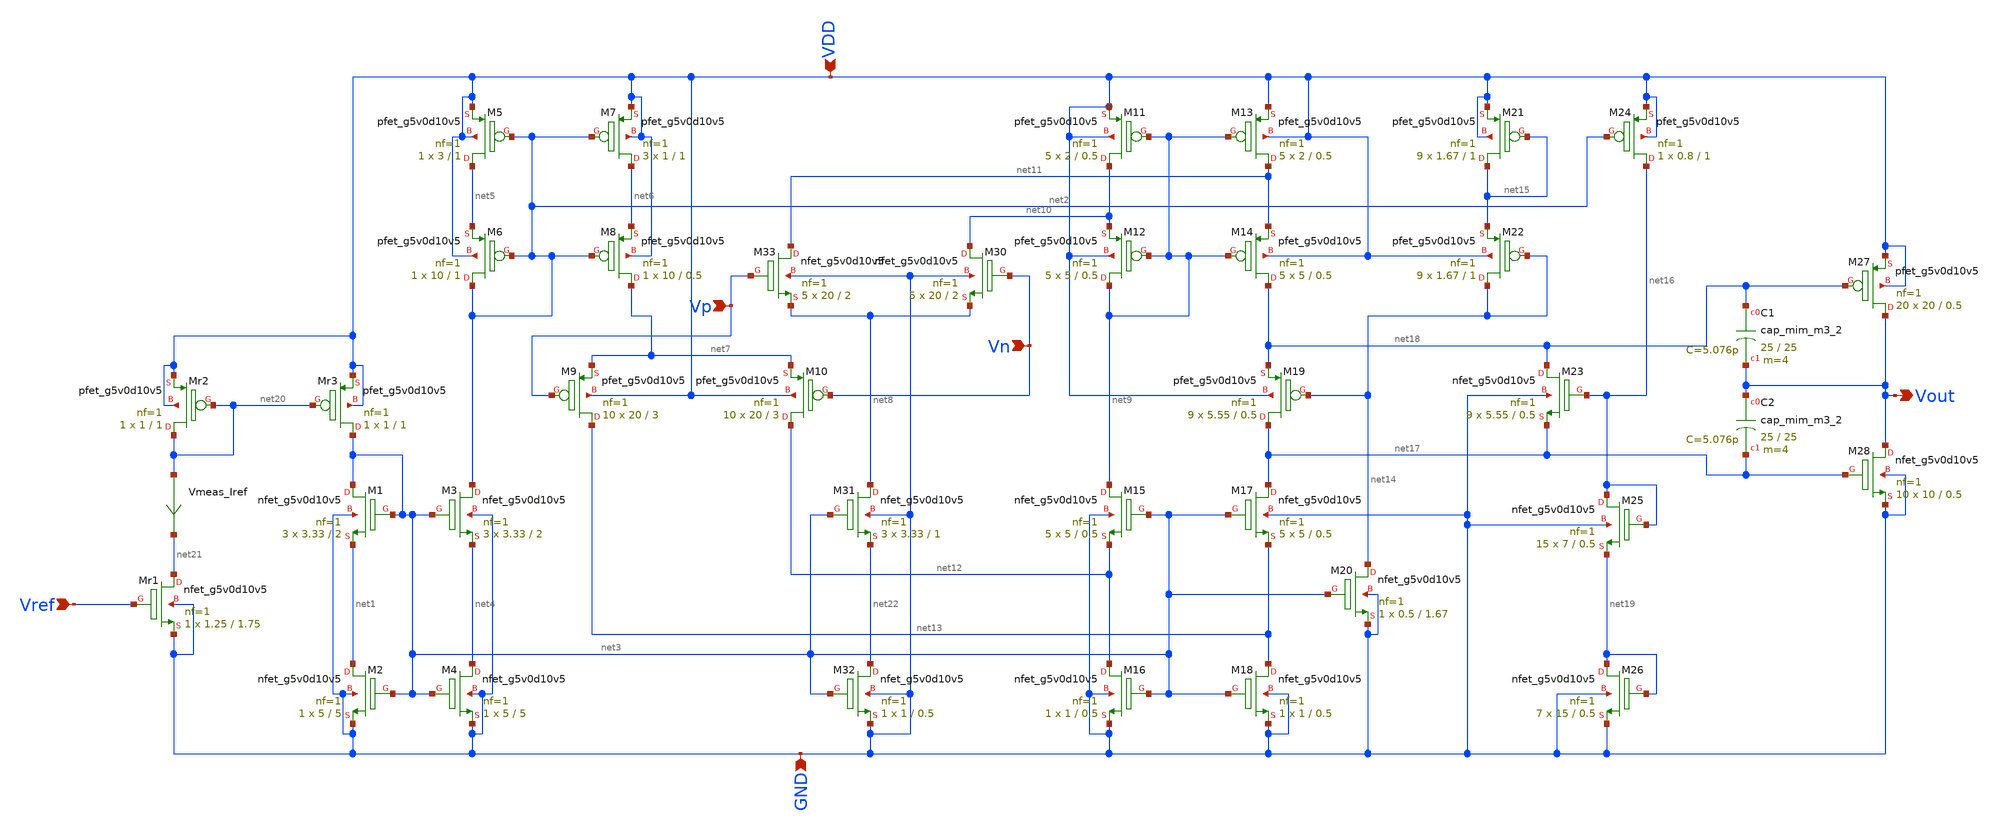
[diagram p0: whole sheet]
** sch_path: xschem/opamp_x.sch
**.subckt opamp_x Vref Vn Vp Vout VDD GND
*.ipin Vref
*.ipin Vn
*.ipin Vp
*.opin Vout
*.ipin VDD
*.ipin GND
XM1 net3 net3 net1 GND sky130_fd_pr__nfet_g5v0d10v5 L=2 W=3.33 nf=1 ad='int((1 + 1)/2) * 3.33 / 1 * 0.29'
+ as='int((1 + 2)/2) * 3.33 / 1 * 0.29' pd='2*int((1 + 1)/2) * (3.33 / 1 + 0.29)' ps='2*int((1 + 2)/2) * (3.33 / 1 + 0.29)'
+ nrd='0.29 / 3.33 ' nrs='0.29 / 3.33 ' sa=0 sb=0 sd=0 mult=3 m=3
XM2 net1 net3 GND GND sky130_fd_pr__nfet_g5v0d10v5 L=5 W=5 nf=1 ad='int((1 + 1)/2) * 5 / 1 * 0.29' as='int((1 + 2)/2) * 5 / 1 * 0.29'
+ pd='2*int((1 + 1)/2) * (5 / 1 + 0.29)' ps='2*int((1 + 2)/2) * (5 / 1 + 0.29)' nrd='0.29 / 5 ' nrs='0.29 / 5 '
+ sa=0 sb=0 sd=0 mult=1 m=1
XM3 net2 net3 net4 GND sky130_fd_pr__nfet_g5v0d10v5 L=2 W=3.33 nf=1 ad='int((1 + 1)/2) * 3.33 / 1 * 0.29'
+ as='int((1 + 2)/2) * 3.33 / 1 * 0.29' pd='2*int((1 + 1)/2) * (3.33 / 1 + 0.29)' ps='2*int((1 + 2)/2) * (3.33 / 1 + 0.29)'
+ nrd='0.29 / 3.33 ' nrs='0.29 / 3.33 ' sa=0 sb=0 sd=0 mult=3 m=3
XM4 net4 net3 GND GND sky130_fd_pr__nfet_g5v0d10v5 L=5 W=5 nf=1 ad='int((1 + 1)/2) * 5 / 1 * 0.29' as='int((1 + 2)/2) * 5 / 1 * 0.29'
+ pd='2*int((1 + 1)/2) * (5 / 1 + 0.29)' ps='2*int((1 + 2)/2) * (5 / 1 + 0.29)' nrd='0.29 / 5 ' nrs='0.29 / 5 '
+ sa=0 sb=0 sd=0 mult=1 m=1
XM5 net5 net2 VDD VDD sky130_fd_pr__pfet_g5v0d10v5 L=1 W=3 nf=1 ad='int((1 + 1)/2) * 3 / 1 * 0.29' as='int((1 + 2)/2) * 3 / 1 * 0.29'
+ pd='2*int((1 + 1)/2) * (3 / 1 + 0.29)' ps='2*int((1 + 2)/2) * (3 / 1 + 0.29)' nrd='0.29 / 3 ' nrs='0.29 / 3 '
+ sa=0 sb=0 sd=0 mult=1 m=1
XM6 net2 net2 net5 VDD sky130_fd_pr__pfet_g5v0d10v5 L=1 W=10 nf=1 ad='int((1 + 1)/2) * 10 / 1 * 0.29'
+ as='int((1 + 2)/2) * 10 / 1 * 0.29' pd='2*int((1 + 1)/2) * (10 / 1 + 0.29)' ps='2*int((1 + 2)/2) * (10 / 1 + 0.29)'
+ nrd='0.29 / 10 ' nrs='0.29 / 10 ' sa=0 sb=0 sd=0 mult=1 m=1
XM7 net6 net2 VDD VDD sky130_fd_pr__pfet_g5v0d10v5 L=1 W=1 nf=1 ad='int((1 + 1)/2) * 1 / 1 * 0.29' as='int((1 + 2)/2) * 1 / 1 * 0.29'
+ pd='2*int((1 + 1)/2) * (1 / 1 + 0.29)' ps='2*int((1 + 2)/2) * (1 / 1 + 0.29)' nrd='0.29 / 1 ' nrs='0.29 / 1 '
+ sa=0 sb=0 sd=0 mult=3 m=3
XM8 net7 net2 net6 VDD sky130_fd_pr__pfet_g5v0d10v5 L=0.5 W=10 nf=1 ad='int((1 + 1)/2) * 10 / 1 * 0.29'
+ as='int((1 + 2)/2) * 10 / 1 * 0.29' pd='2*int((1 + 1)/2) * (10 / 1 + 0.29)' ps='2*int((1 + 2)/2) * (10 / 1 + 0.29)'
+ nrd='0.29 / 10 ' nrs='0.29 / 10 ' sa=0 sb=0 sd=0 mult=1 m=1
XM9 net13 Vp net7 VDD sky130_fd_pr__pfet_g5v0d10v5 L=3 W=20 nf=1 ad='int((1 + 1)/2) * 20 / 1 * 0.29'
+ as='int((1 + 2)/2) * 20 / 1 * 0.29' pd='2*int((1 + 1)/2) * (20 / 1 + 0.29)' ps='2*int((1 + 2)/2) * (20 / 1 + 0.29)'
+ nrd='0.29 / 20 ' nrs='0.29 / 20 ' sa=0 sb=0 sd=0 mult=10 m=10
XM10 net12 Vn net7 VDD sky130_fd_pr__pfet_g5v0d10v5 L=3 W=20 nf=1 ad='int((1 + 1)/2) * 20 / 1 * 0.29'
+ as='int((1 + 2)/2) * 20 / 1 * 0.29' pd='2*int((1 + 1)/2) * (20 / 1 + 0.29)' ps='2*int((1 + 2)/2) * (20 / 1 + 0.29)'
+ nrd='0.29 / 20 ' nrs='0.29 / 20 ' sa=0 sb=0 sd=0 mult=10 m=10
XM11 net10 net9 VDD VDD sky130_fd_pr__pfet_g5v0d10v5 L=0.5 W=2 nf=1 ad='int((1 + 1)/2) * 2 / 1 * 0.29'
+ as='int((1 + 2)/2) * 2 / 1 * 0.29' pd='2*int((1 + 1)/2) * (2 / 1 + 0.29)' ps='2*int((1 + 2)/2) * (2 / 1 + 0.29)'
+ nrd='0.29 / 2 ' nrs='0.29 / 2 ' sa=0 sb=0 sd=0 mult=5 m=5
XM12 net9 net9 net10 VDD sky130_fd_pr__pfet_g5v0d10v5 L=0.5 W=5 nf=1 ad='int((1 + 1)/2) * 5 / 1 * 0.29'
+ as='int((1 + 2)/2) * 5 / 1 * 0.29' pd='2*int((1 + 1)/2) * (5 / 1 + 0.29)' ps='2*int((1 + 2)/2) * (5 / 1 + 0.29)'
+ nrd='0.29 / 5 ' nrs='0.29 / 5 ' sa=0 sb=0 sd=0 mult=5 m=5
XM13 net11 net9 VDD VDD sky130_fd_pr__pfet_g5v0d10v5 L=0.5 W=2 nf=1 ad='int((1 + 1)/2) * 2 / 1 * 0.29'
+ as='int((1 + 2)/2) * 2 / 1 * 0.29' pd='2*int((1 + 1)/2) * (2 / 1 + 0.29)' ps='2*int((1 + 2)/2) * (2 / 1 + 0.29)'
+ nrd='0.29 / 2 ' nrs='0.29 / 2 ' sa=0 sb=0 sd=0 mult=5 m=5
XM14 net18 net9 net11 VDD sky130_fd_pr__pfet_g5v0d10v5 L=0.5 W=5 nf=1 ad='int((1 + 1)/2) * 5 / 1 * 0.29'
+ as='int((1 + 2)/2) * 5 / 1 * 0.29' pd='2*int((1 + 1)/2) * (5 / 1 + 0.29)' ps='2*int((1 + 2)/2) * (5 / 1 + 0.29)'
+ nrd='0.29 / 5 ' nrs='0.29 / 5 ' sa=0 sb=0 sd=0 mult=5 m=5
XM15 net9 net3 net12 GND sky130_fd_pr__nfet_g5v0d10v5 L=0.5 W=5 nf=1 ad='int((1 + 1)/2) * 5 / 1 * 0.29'
+ as='int((1 + 2)/2) * 5 / 1 * 0.29' pd='2*int((1 + 1)/2) * (5 / 1 + 0.29)' ps='2*int((1 + 2)/2) * (5 / 1 + 0.29)'
+ nrd='0.29 / 5 ' nrs='0.29 / 5 ' sa=0 sb=0 sd=0 mult=5 m=5
XM16 net12 net3 GND GND sky130_fd_pr__nfet_g5v0d10v5 L=0.5 W=1 nf=1 ad='int((1 + 1)/2) * 1 / 1 * 0.29'
+ as='int((1 + 2)/2) * 1 / 1 * 0.29' pd='2*int((1 + 1)/2) * (1 / 1 + 0.29)' ps='2*int((1 + 2)/2) * (1 / 1 + 0.29)'
+ nrd='0.29 / 1 ' nrs='0.29 / 1 ' sa=0 sb=0 sd=0 mult=1 m=1
XM17 net17 net3 net13 GND sky130_fd_pr__nfet_g5v0d10v5 L=0.5 W=5 nf=1 ad='int((1 + 1)/2) * 5 / 1 * 0.29'
+ as='int((1 + 2)/2) * 5 / 1 * 0.29' pd='2*int((1 + 1)/2) * (5 / 1 + 0.29)' ps='2*int((1 + 2)/2) * (5 / 1 + 0.29)'
+ nrd='0.29 / 5 ' nrs='0.29 / 5 ' sa=0 sb=0 sd=0 mult=5 m=5
XM18 net13 net3 GND GND sky130_fd_pr__nfet_g5v0d10v5 L=0.5 W=1 nf=1 ad='int((1 + 1)/2) * 1 / 1 * 0.29'
+ as='int((1 + 2)/2) * 1 / 1 * 0.29' pd='2*int((1 + 1)/2) * (1 / 1 + 0.29)' ps='2*int((1 + 2)/2) * (1 / 1 + 0.29)'
+ nrd='0.29 / 1 ' nrs='0.29 / 1 ' sa=0 sb=0 sd=0 mult=1 m=1
XM19 net17 net14 net18 VDD sky130_fd_pr__pfet_g5v0d10v5 L=0.5 W=5.55 nf=1 ad='int((1 + 1)/2) * 5.55 / 1 * 0.29'
+ as='int((1 + 2)/2) * 5.55 / 1 * 0.29' pd='2*int((1 + 1)/2) * (5.55 / 1 + 0.29)' ps='2*int((1 + 2)/2) * (5.55 / 1 + 0.29)'
+ nrd='0.29 / 5.55 ' nrs='0.29 / 5.55 ' sa=0 sb=0 sd=0 mult=9 m=9
XM20 net14 net3 GND GND sky130_fd_pr__nfet_g5v0d10v5 L=1.67 W=0.5 nf=1 ad='int((1 + 1)/2) * 0.5 / 1 * 0.29'
+ as='int((1 + 2)/2) * 0.5 / 1 * 0.29' pd='2*int((1 + 1)/2) * (0.5 / 1 + 0.29)' ps='2*int((1 + 2)/2) * (0.5 / 1 + 0.29)'
+ nrd='0.29 / 0.5 ' nrs='0.29 / 0.5 ' sa=0 sb=0 sd=0 mult=1 m=1
XM21 net15 net15 VDD VDD sky130_fd_pr__pfet_g5v0d10v5 L=1 W=1.67 nf=1 ad='int((1 + 1)/2) * 1.67 / 1 * 0.29'
+ as='int((1 + 2)/2) * 1.67 / 1 * 0.29' pd='2*int((1 + 1)/2) * (1.67 / 1 + 0.29)' ps='2*int((1 + 2)/2) * (1.67 / 1 + 0.29)'
+ nrd='0.29 / 1.67 ' nrs='0.29 / 1.67 ' sa=0 sb=0 sd=0 mult=9 m=9
XM22 net14 net14 net15 VDD sky130_fd_pr__pfet_g5v0d10v5 L=1 W=1.67 nf=1 ad='int((1 + 1)/2) * 1.67 / 1 * 0.29'
+ as='int((1 + 2)/2) * 1.67 / 1 * 0.29' pd='2*int((1 + 1)/2) * (1.67 / 1 + 0.29)' ps='2*int((1 + 2)/2) * (1.67 / 1 + 0.29)'
+ nrd='0.29 / 1.67 ' nrs='0.29 / 1.67 ' sa=0 sb=0 sd=0 mult=9 m=9
XM24 net16 net2 VDD VDD sky130_fd_pr__pfet_g5v0d10v5 L=1 W=0.8 nf=1 ad='int((1 + 1)/2) * 0.8 / 1 * 0.29'
+ as='int((1 + 2)/2) * 0.8 / 1 * 0.29' pd='2*int((1 + 1)/2) * (0.8 / 1 + 0.29)' ps='2*int((1 + 2)/2) * (0.8 / 1 + 0.29)'
+ nrd='0.29 / 0.8 ' nrs='0.29 / 0.8 ' sa=0 sb=0 sd=0 mult=1 m=1
XM25 net16 net16 net19 GND sky130_fd_pr__nfet_g5v0d10v5 L=0.5 W=7 nf=1 ad='int((1 + 1)/2) * 7 / 1 * 0.29'
+ as='int((1 + 2)/2) * 7 / 1 * 0.29' pd='2*int((1 + 1)/2) * (7 / 1 + 0.29)' ps='2*int((1 + 2)/2) * (7 / 1 + 0.29)'
+ nrd='0.29 / 7 ' nrs='0.29 / 7 ' sa=0 sb=0 sd=0 mult=15 m=15
XM26 net19 net19 GND GND sky130_fd_pr__nfet_g5v0d10v5 L=0.5 W=15 nf=1 ad='int((1 + 1)/2) * 15 / 1 * 0.29'
+ as='int((1 + 2)/2) * 15 / 1 * 0.29' pd='2*int((1 + 1)/2) * (15 / 1 + 0.29)' ps='2*int((1 + 2)/2) * (15 / 1 + 0.29)'
+ nrd='0.29 / 15 ' nrs='0.29 / 15 ' sa=0 sb=0 sd=0 mult=7 m=7
XM27 Vout net18 VDD VDD sky130_fd_pr__pfet_g5v0d10v5 L=0.5 W=20 nf=1 ad='int((1 + 1)/2) * 20 / 1 * 0.29'
+ as='int((1 + 2)/2) * 20 / 1 * 0.29' pd='2*int((1 + 1)/2) * (20 / 1 + 0.29)' ps='2*int((1 + 2)/2) * (20 / 1 + 0.29)'
+ nrd='0.29 / 20 ' nrs='0.29 / 20 ' sa=0 sb=0 sd=0 mult=20 m=20
XM28 Vout net17 GND GND sky130_fd_pr__nfet_g5v0d10v5 L=0.5 W=10 nf=1 ad='int((1 + 1)/2) * 10 / 1 * 0.29'
+ as='int((1 + 2)/2) * 10 / 1 * 0.29' pd='2*int((1 + 1)/2) * (10 / 1 + 0.29)' ps='2*int((1 + 2)/2) * (10 / 1 + 0.29)'
+ nrd='0.29 / 10 ' nrs='0.29 / 10 ' sa=0 sb=0 sd=0 mult=10 m=10
XM33 net11 Vp net8 GND sky130_fd_pr__nfet_g5v0d10v5 L=2 W=20 nf=1 ad='int((1 + 1)/2) * 20 / 1 * 0.29'
+ as='int((1 + 2)/2) * 20 / 1 * 0.29' pd='2*int((1 + 1)/2) * (20 / 1 + 0.29)' ps='2*int((1 + 2)/2) * (20 / 1 + 0.29)'
+ nrd='0.29 / 20 ' nrs='0.29 / 20 ' sa=0 sb=0 sd=0 mult=5 m=5
XM30 net10 Vn net8 GND sky130_fd_pr__nfet_g5v0d10v5 L=2 W=20 nf=1 ad='int((1 + 1)/2) * 20 / 1 * 0.29'
+ as='int((1 + 2)/2) * 20 / 1 * 0.29' pd='2*int((1 + 1)/2) * (20 / 1 + 0.29)' ps='2*int((1 + 2)/2) * (20 / 1 + 0.29)'
+ nrd='0.29 / 20 ' nrs='0.29 / 20 ' sa=0 sb=0 sd=0 mult=5 m=5
XM31 net8 net3 net22 GND sky130_fd_pr__nfet_g5v0d10v5 L=1 W=3.33 nf=1 ad='int((1 + 1)/2) * 3.33 / 1 * 0.29'
+ as='int((1 + 2)/2) * 3.33 / 1 * 0.29' pd='2*int((1 + 1)/2) * (3.33 / 1 + 0.29)' ps='2*int((1 + 2)/2) * (3.33 / 1 + 0.29)'
+ nrd='0.29 / 3.33 ' nrs='0.29 / 3.33 ' sa=0 sb=0 sd=0 mult=3 m=3
XM32 net22 net3 GND GND sky130_fd_pr__nfet_g5v0d10v5 L=0.5 W=1 nf=1 ad='int((1 + 1)/2) * 1 / 1 * 0.29'
+ as='int((1 + 2)/2) * 1 / 1 * 0.29' pd='2*int((1 + 1)/2) * (1 / 1 + 0.29)' ps='2*int((1 + 2)/2) * (1 / 1 + 0.29)'
+ nrd='0.29 / 1 ' nrs='0.29 / 1 ' sa=0 sb=0 sd=0 mult=1 m=1
XM23 net18 net16 net17 GND sky130_fd_pr__nfet_g5v0d10v5 L=0.5 W=5.55 nf=1 ad='int((1 + 1)/2) * 5.55 / 1 * 0.29'
+ as='int((1 + 2)/2) * 5.55 / 1 * 0.29' pd='2*int((1 + 1)/2) * (5.55 / 1 + 0.29)' ps='2*int((1 + 2)/2) * (5.55 / 1 + 0.29)'
+ nrd='0.29 / 5.55 ' nrs='0.29 / 5.55 ' sa=0 sb=0 sd=0 mult=9 m=9
XMr1 net21 Vref GND GND sky130_fd_pr__nfet_g5v0d10v5 L=1.75 W=1.25 nf=1 ad='int((1 + 1)/2) * 1.25 / 1 * 0.29'
+ as='int((1 + 2)/2) * 1.25 / 1 * 0.29' pd='2*int((1 + 1)/2) * (1.25 / 1 + 0.29)' ps='2*int((1 + 2)/2) * (1.25 / 1 + 0.29)'
+ nrd='0.29 / 1.25 ' nrs='0.29 / 1.25 ' sa=0 sb=0 sd=0 mult=1 m=1
XMr2 net20 net20 VDD VDD sky130_fd_pr__pfet_g5v0d10v5 L=1 W=1 nf=1 ad='int((1 + 1)/2) * 1 / 1 * 0.29'
+ as='int((1 + 2)/2) * 1 / 1 * 0.29' pd='2*int((1 + 1)/2) * (1 / 1 + 0.29)' ps='2*int((1 + 2)/2) * (1 / 1 + 0.29)'
+ nrd='0.29 / 1 ' nrs='0.29 / 1 ' sa=0 sb=0 sd=0 mult=1 m=1
XMr3 net3 net20 VDD VDD sky130_fd_pr__pfet_g5v0d10v5 L=1 W=1 nf=1 ad='int((1 + 1)/2) * 1 / 1 * 0.29'
+ as='int((1 + 2)/2) * 1 / 1 * 0.29' pd='2*int((1 + 1)/2) * (1 / 1 + 0.29)' ps='2*int((1 + 2)/2) * (1 / 1 + 0.29)'
+ nrd='0.29 / 1 ' nrs='0.29 / 1 ' sa=0 sb=0 sd=0 mult=1 m=1
Vmeas_Iref net20 net21 0
.save i(vmeas_iref)
XC2 Vout net17 sky130_fd_pr__cap_mim_m3_2 W=25 L=25 MF=4 m=4
XC1 net18 Vout sky130_fd_pr__cap_mim_m3_2 W=25 L=25 MF=4 m=4
**.ends
.end
